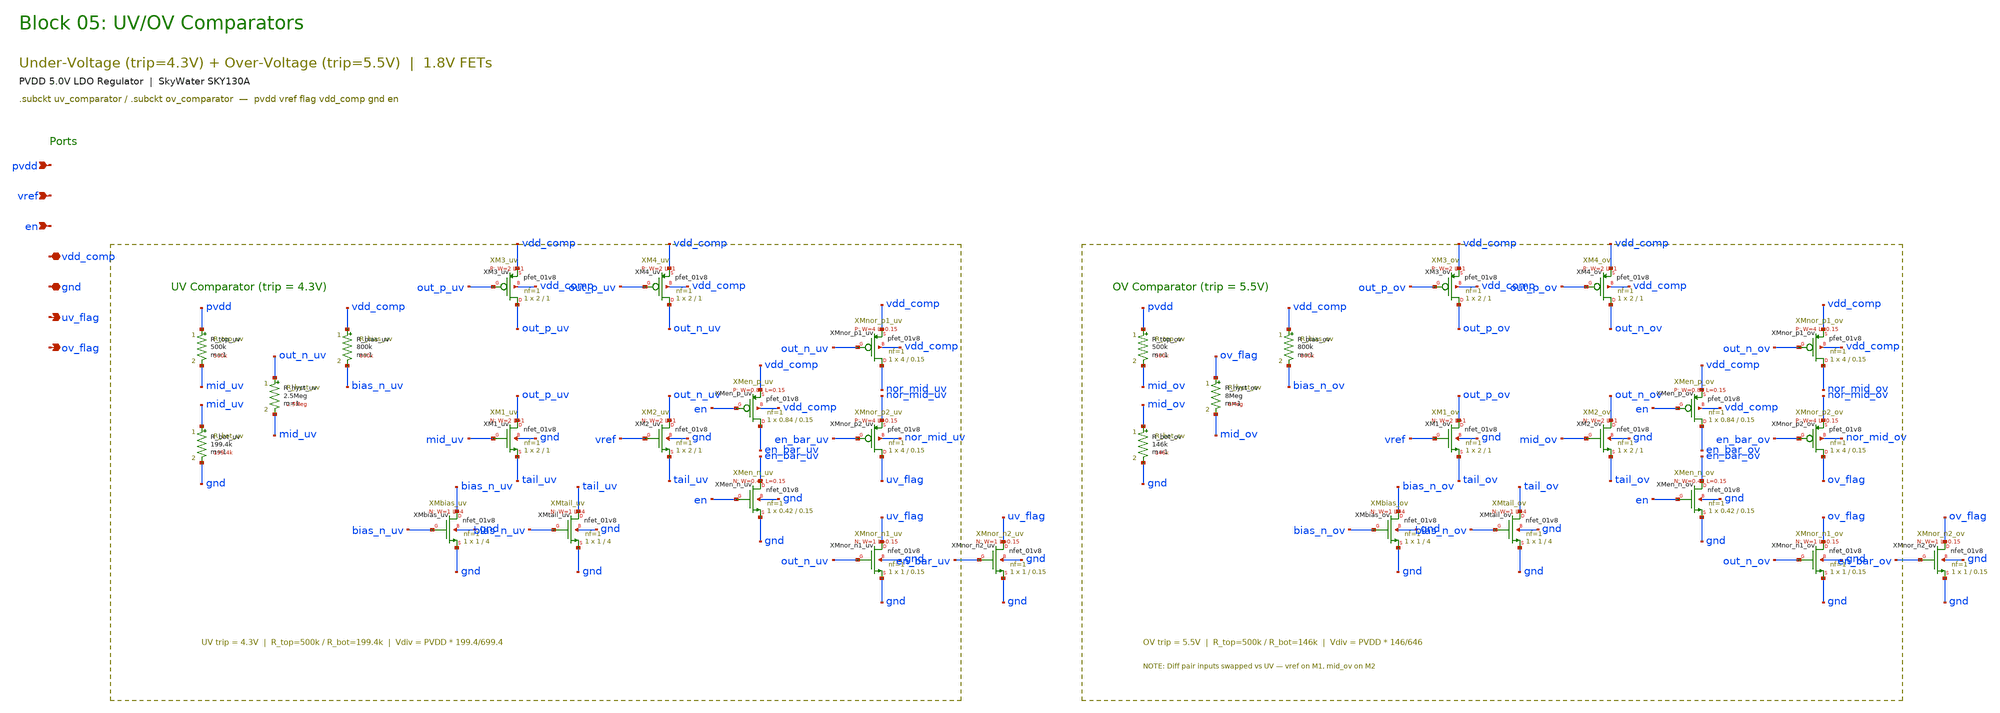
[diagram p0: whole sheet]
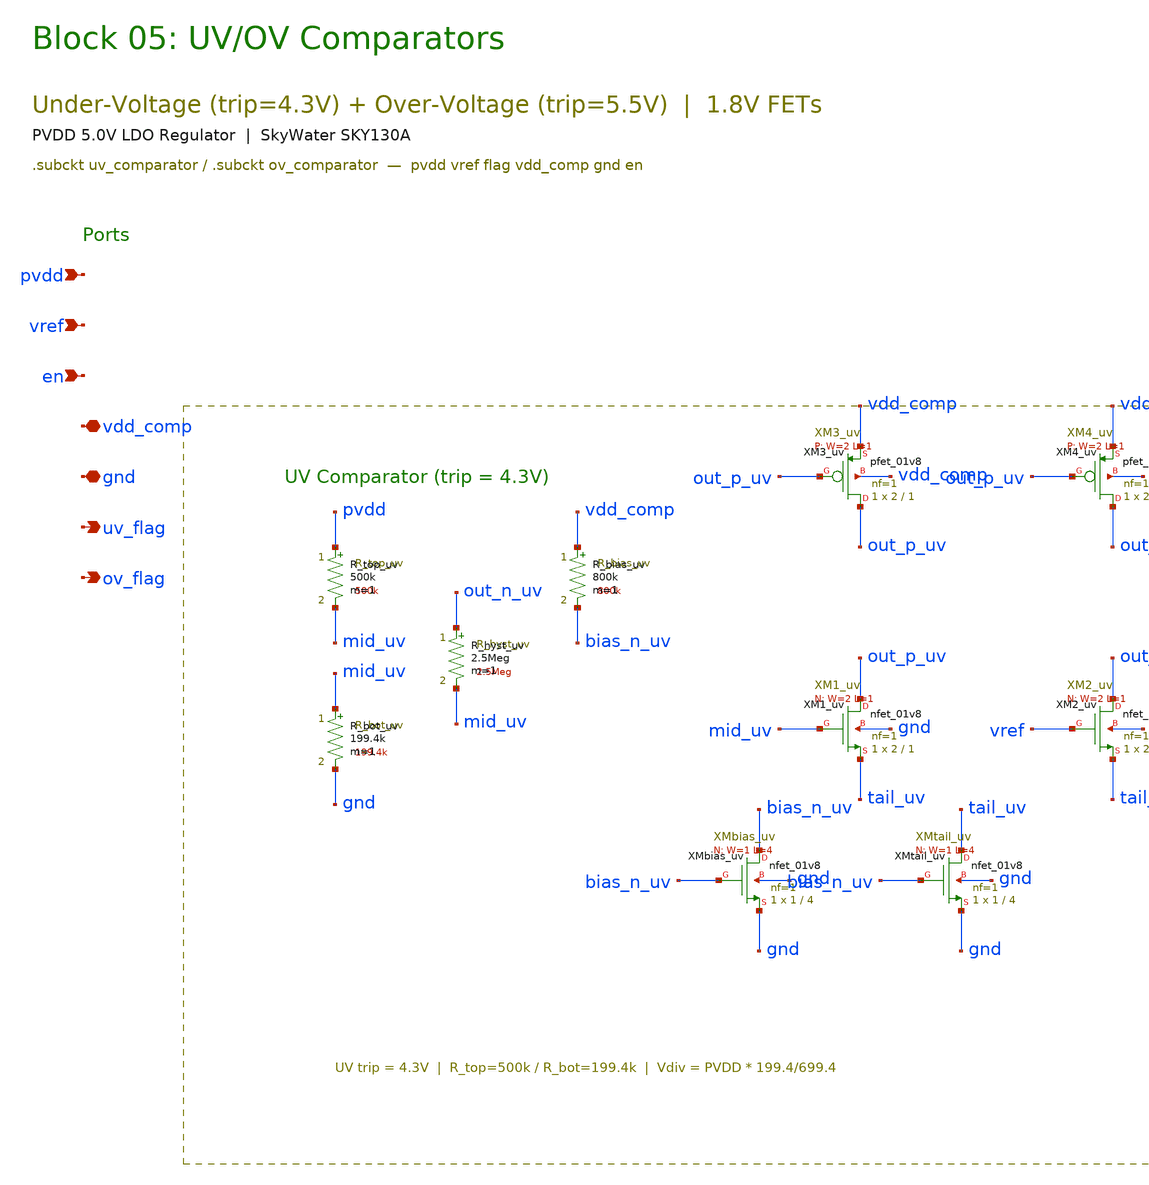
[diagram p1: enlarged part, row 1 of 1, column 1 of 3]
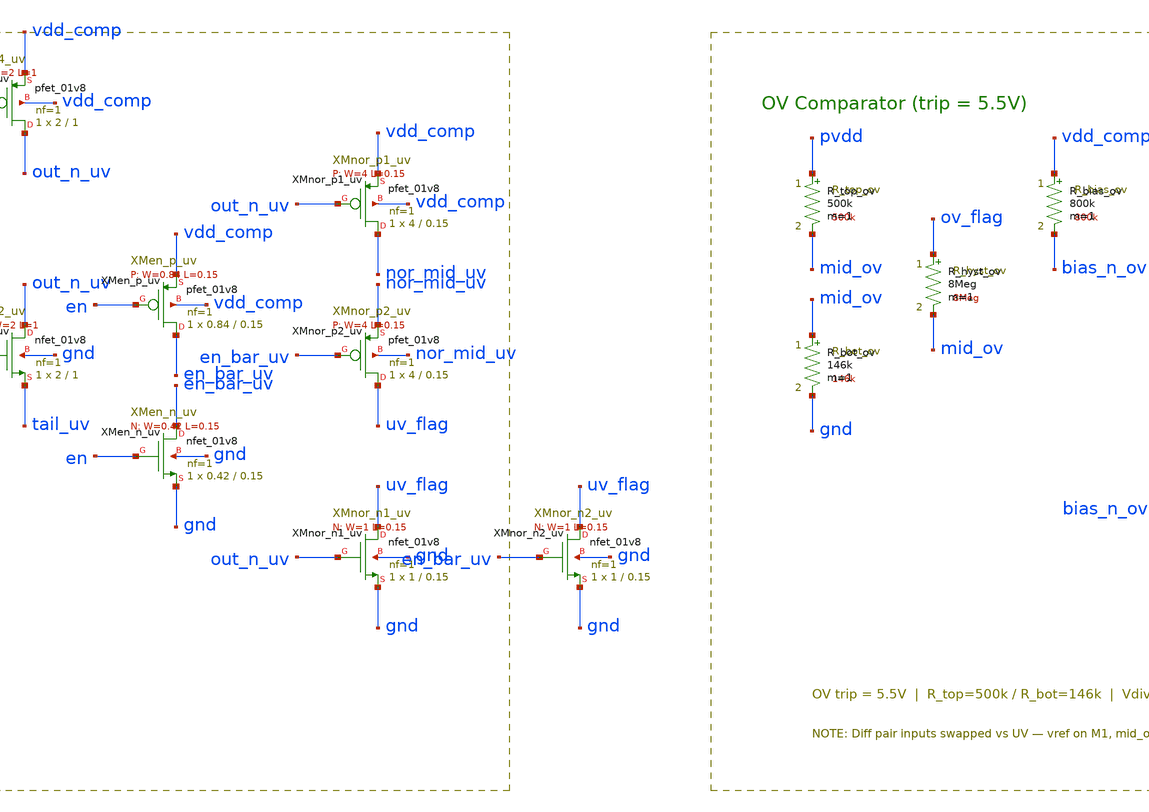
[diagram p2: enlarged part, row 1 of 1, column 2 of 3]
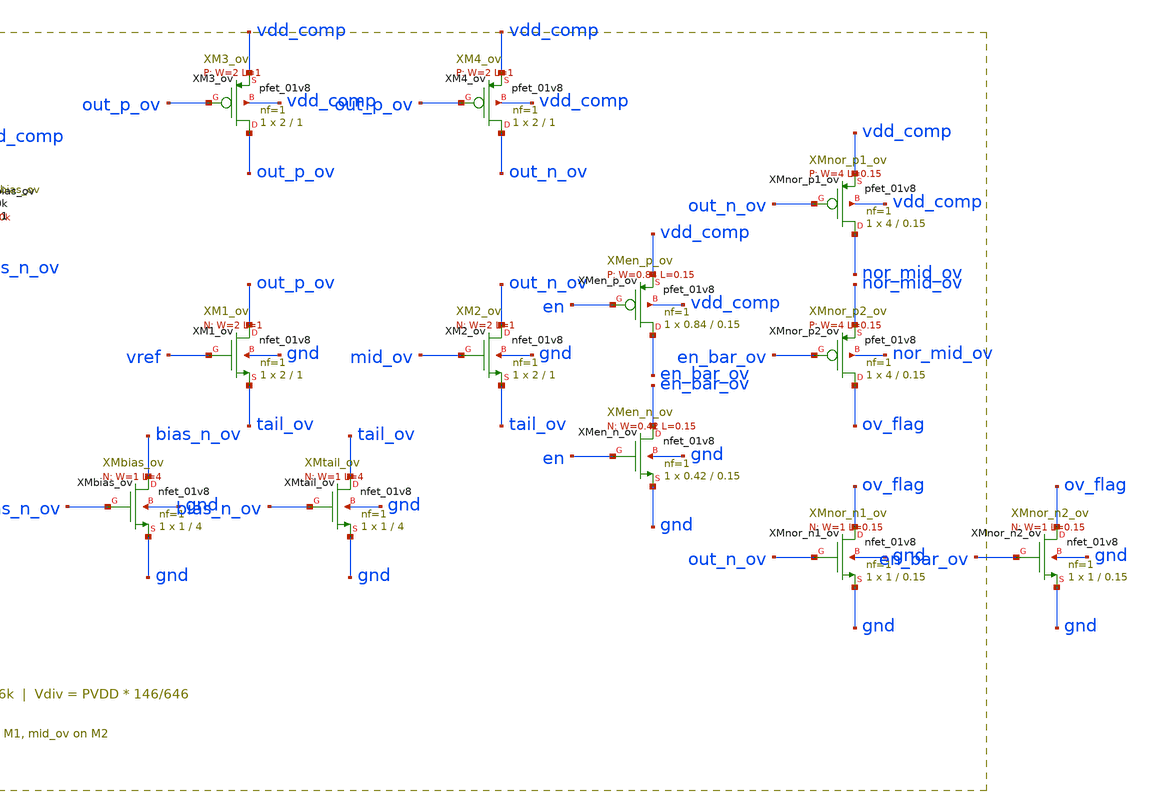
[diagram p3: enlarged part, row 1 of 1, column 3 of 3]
** sch_path: pvdd_regulator/10_top_integration/schematics/pvdd_05_uv_ov.sch
**.subckt pvdd_05_uv_ov pvdd vref en vdd_comp gnd uv_flag ov_flag
*.ipin pvdd
*.ipin vref
*.ipin en
*.iopin vdd_comp
*.iopin gnd
*.opin uv_flag
*.opin ov_flag
R_top_uv pvdd mid_uv 500k m=1
R_bot_uv mid_uv gnd 199.4k m=1
R_hyst_uv out_n_uv mid_uv 2.5Meg m=1
R_bias_uv vdd_comp bias_n_uv 800k m=1
XXMbias_uv bias_n_uv bias_n_uv gnd gnd sky130_fd_pr__nfet_01v8 L=4 W=1 nf=1 ad='int((1 + 1)/2) * 1 / 1 * 0.29'
+ as='int((1 + 2)/2) * 1 / 1 * 0.29' pd='2*int((1 + 1)/2) * (1 / 1 + 0.29)' ps='2*int((1 + 2)/2) * (1 / 1 + 0.29)'
+ nrd='0.29 / 1 ' nrs='0.29 / 1 ' sa=0 sb=0 sd=0 mult=1 m=1
XXMtail_uv tail_uv bias_n_uv gnd gnd sky130_fd_pr__nfet_01v8 L=4 W=1 nf=1 ad='int((1 + 1)/2) * 1 / 1 * 0.29'
+ as='int((1 + 2)/2) * 1 / 1 * 0.29' pd='2*int((1 + 1)/2) * (1 / 1 + 0.29)' ps='2*int((1 + 2)/2) * (1 / 1 + 0.29)'
+ nrd='0.29 / 1 ' nrs='0.29 / 1 ' sa=0 sb=0 sd=0 mult=1 m=1
XXM1_uv out_p_uv mid_uv tail_uv gnd sky130_fd_pr__nfet_01v8 L=1 W=2 nf=1 ad='int((1 + 1)/2) * 2 / 1 * 0.29'
+ as='int((1 + 2)/2) * 2 / 1 * 0.29' pd='2*int((1 + 1)/2) * (2 / 1 + 0.29)' ps='2*int((1 + 2)/2) * (2 / 1 + 0.29)'
+ nrd='0.29 / 2 ' nrs='0.29 / 2 ' sa=0 sb=0 sd=0 mult=1 m=1
XXM2_uv out_n_uv vref tail_uv gnd sky130_fd_pr__nfet_01v8 L=1 W=2 nf=1 ad='int((1 + 1)/2) * 2 / 1 * 0.29'
+ as='int((1 + 2)/2) * 2 / 1 * 0.29' pd='2*int((1 + 1)/2) * (2 / 1 + 0.29)' ps='2*int((1 + 2)/2) * (2 / 1 + 0.29)'
+ nrd='0.29 / 2 ' nrs='0.29 / 2 ' sa=0 sb=0 sd=0 mult=1 m=1
XXM3_uv out_p_uv out_p_uv vdd_comp vdd_comp sky130_fd_pr__pfet_01v8 L=1 W=2 nf=1 ad='int((nf+1)/2) * W/nf * 0.29'
+ as='int((nf+2)/2) * W/nf * 0.29' pd='2*int((nf+1)/2) * (W/nf + 0.29)' ps='2*int((nf+2)/2) * (W/nf + 0.29)'
+ nrd='0.29 / W' nrs='0.29 / W' sa=0 sb=0 sd=0 mult=1 m=1
XXM4_uv out_n_uv out_p_uv vdd_comp vdd_comp sky130_fd_pr__pfet_01v8 L=1 W=2 nf=1 ad='int((nf+1)/2) * W/nf * 0.29'
+ as='int((nf+2)/2) * W/nf * 0.29' pd='2*int((nf+1)/2) * (W/nf + 0.29)' ps='2*int((nf+2)/2) * (W/nf + 0.29)'
+ nrd='0.29 / W' nrs='0.29 / W' sa=0 sb=0 sd=0 mult=1 m=1
XXMen_n_uv en_bar_uv en gnd gnd sky130_fd_pr__nfet_01v8 L=0.15 W=0.42 nf=1 ad='int((1 + 1)/2) * 0.42 / 1 * 0.29'
+ as='int((1 + 2)/2) * 0.42 / 1 * 0.29' pd='2*int((1 + 1)/2) * (0.42 / 1 + 0.29)' ps='2*int((1 + 2)/2) * (0.42 / 1 + 0.29)'
+ nrd='0.29 / 0.42 ' nrs='0.29 / 0.42 ' sa=0 sb=0 sd=0 mult=1 m=1
XXMen_p_uv en_bar_uv en vdd_comp vdd_comp sky130_fd_pr__pfet_01v8 L=0.15 W=0.84 nf=1 ad='int((nf+1)/2) * W/nf * 0.29'
+ as='int((nf+2)/2) * W/nf * 0.29' pd='2*int((nf+1)/2) * (W/nf + 0.29)' ps='2*int((nf+2)/2) * (W/nf + 0.29)'
+ nrd='0.29 / W' nrs='0.29 / W' sa=0 sb=0 sd=0 mult=1 m=1
XXMnor_p1_uv nor_mid_uv out_n_uv vdd_comp vdd_comp sky130_fd_pr__pfet_01v8 L=0.15 W=4 nf=1 ad='int((nf+1)/2) * W/nf * 0.29'
+ as='int((nf+2)/2) * W/nf * 0.29' pd='2*int((nf+1)/2) * (W/nf + 0.29)' ps='2*int((nf+2)/2) * (W/nf + 0.29)'
+ nrd='0.29 / W' nrs='0.29 / W' sa=0 sb=0 sd=0 mult=1 m=1
XXMnor_p2_uv uv_flag en_bar_uv nor_mid_uv nor_mid_uv sky130_fd_pr__pfet_01v8 L=0.15 W=4 nf=1 ad='int((nf+1)/2) * W/nf * 0.29'
+ as='int((nf+2)/2) * W/nf * 0.29' pd='2*int((nf+1)/2) * (W/nf + 0.29)' ps='2*int((nf+2)/2) * (W/nf + 0.29)'
+ nrd='0.29 / W' nrs='0.29 / W' sa=0 sb=0 sd=0 mult=1 m=1
XXMnor_n1_uv uv_flag out_n_uv gnd gnd sky130_fd_pr__nfet_01v8 L=0.15 W=1 nf=1 ad='int((1 + 1)/2) * 1 / 1 * 0.29'
+ as='int((1 + 2)/2) * 1 / 1 * 0.29' pd='2*int((1 + 1)/2) * (1 / 1 + 0.29)' ps='2*int((1 + 2)/2) * (1 / 1 + 0.29)'
+ nrd='0.29 / 1 ' nrs='0.29 / 1 ' sa=0 sb=0 sd=0 mult=1 m=1
XXMnor_n2_uv uv_flag en_bar_uv gnd gnd sky130_fd_pr__nfet_01v8 L=0.15 W=1 nf=1 ad='int((1 + 1)/2) * 1 / 1 * 0.29'
+ as='int((1 + 2)/2) * 1 / 1 * 0.29' pd='2*int((1 + 1)/2) * (1 / 1 + 0.29)' ps='2*int((1 + 2)/2) * (1 / 1 + 0.29)'
+ nrd='0.29 / 1 ' nrs='0.29 / 1 ' sa=0 sb=0 sd=0 mult=1 m=1
R_top_ov pvdd mid_ov 500k m=1
R_bot_ov mid_ov gnd 146k m=1
R_hyst_ov ov_flag mid_ov 8Meg m=1
R_bias_ov vdd_comp bias_n_ov 800k m=1
XXMbias_ov bias_n_ov bias_n_ov gnd gnd sky130_fd_pr__nfet_01v8 L=4 W=1 nf=1 ad='int((1 + 1)/2) * 1 / 1 * 0.29'
+ as='int((1 + 2)/2) * 1 / 1 * 0.29' pd='2*int((1 + 1)/2) * (1 / 1 + 0.29)' ps='2*int((1 + 2)/2) * (1 / 1 + 0.29)'
+ nrd='0.29 / 1 ' nrs='0.29 / 1 ' sa=0 sb=0 sd=0 mult=1 m=1
XXMtail_ov tail_ov bias_n_ov gnd gnd sky130_fd_pr__nfet_01v8 L=4 W=1 nf=1 ad='int((1 + 1)/2) * 1 / 1 * 0.29'
+ as='int((1 + 2)/2) * 1 / 1 * 0.29' pd='2*int((1 + 1)/2) * (1 / 1 + 0.29)' ps='2*int((1 + 2)/2) * (1 / 1 + 0.29)'
+ nrd='0.29 / 1 ' nrs='0.29 / 1 ' sa=0 sb=0 sd=0 mult=1 m=1
XXM1_ov out_p_ov vref tail_ov gnd sky130_fd_pr__nfet_01v8 L=1 W=2 nf=1 ad='int((1 + 1)/2) * 2 / 1 * 0.29'
+ as='int((1 + 2)/2) * 2 / 1 * 0.29' pd='2*int((1 + 1)/2) * (2 / 1 + 0.29)' ps='2*int((1 + 2)/2) * (2 / 1 + 0.29)'
+ nrd='0.29 / 2 ' nrs='0.29 / 2 ' sa=0 sb=0 sd=0 mult=1 m=1
XXM2_ov out_n_ov mid_ov tail_ov gnd sky130_fd_pr__nfet_01v8 L=1 W=2 nf=1 ad='int((1 + 1)/2) * 2 / 1 * 0.29'
+ as='int((1 + 2)/2) * 2 / 1 * 0.29' pd='2*int((1 + 1)/2) * (2 / 1 + 0.29)' ps='2*int((1 + 2)/2) * (2 / 1 + 0.29)'
+ nrd='0.29 / 2 ' nrs='0.29 / 2 ' sa=0 sb=0 sd=0 mult=1 m=1
XXM3_ov out_p_ov out_p_ov vdd_comp vdd_comp sky130_fd_pr__pfet_01v8 L=1 W=2 nf=1 ad='int((nf+1)/2) * W/nf * 0.29'
+ as='int((nf+2)/2) * W/nf * 0.29' pd='2*int((nf+1)/2) * (W/nf + 0.29)' ps='2*int((nf+2)/2) * (W/nf + 0.29)'
+ nrd='0.29 / W' nrs='0.29 / W' sa=0 sb=0 sd=0 mult=1 m=1
XXM4_ov out_n_ov out_p_ov vdd_comp vdd_comp sky130_fd_pr__pfet_01v8 L=1 W=2 nf=1 ad='int((nf+1)/2) * W/nf * 0.29'
+ as='int((nf+2)/2) * W/nf * 0.29' pd='2*int((nf+1)/2) * (W/nf + 0.29)' ps='2*int((nf+2)/2) * (W/nf + 0.29)'
+ nrd='0.29 / W' nrs='0.29 / W' sa=0 sb=0 sd=0 mult=1 m=1
XXMen_n_ov en_bar_ov en gnd gnd sky130_fd_pr__nfet_01v8 L=0.15 W=0.42 nf=1 ad='int((1 + 1)/2) * 0.42 / 1 * 0.29'
+ as='int((1 + 2)/2) * 0.42 / 1 * 0.29' pd='2*int((1 + 1)/2) * (0.42 / 1 + 0.29)' ps='2*int((1 + 2)/2) * (0.42 / 1 + 0.29)'
+ nrd='0.29 / 0.42 ' nrs='0.29 / 0.42 ' sa=0 sb=0 sd=0 mult=1 m=1
XXMen_p_ov en_bar_ov en vdd_comp vdd_comp sky130_fd_pr__pfet_01v8 L=0.15 W=0.84 nf=1 ad='int((nf+1)/2) * W/nf * 0.29'
+ as='int((nf+2)/2) * W/nf * 0.29' pd='2*int((nf+1)/2) * (W/nf + 0.29)' ps='2*int((nf+2)/2) * (W/nf + 0.29)'
+ nrd='0.29 / W' nrs='0.29 / W' sa=0 sb=0 sd=0 mult=1 m=1
XXMnor_p1_ov nor_mid_ov out_n_ov vdd_comp vdd_comp sky130_fd_pr__pfet_01v8 L=0.15 W=4 nf=1 ad='int((nf+1)/2) * W/nf * 0.29'
+ as='int((nf+2)/2) * W/nf * 0.29' pd='2*int((nf+1)/2) * (W/nf + 0.29)' ps='2*int((nf+2)/2) * (W/nf + 0.29)'
+ nrd='0.29 / W' nrs='0.29 / W' sa=0 sb=0 sd=0 mult=1 m=1
XXMnor_p2_ov ov_flag en_bar_ov nor_mid_ov nor_mid_ov sky130_fd_pr__pfet_01v8 L=0.15 W=4 nf=1 ad='int((nf+1)/2) * W/nf * 0.29'
+ as='int((nf+2)/2) * W/nf * 0.29' pd='2*int((nf+1)/2) * (W/nf + 0.29)' ps='2*int((nf+2)/2) * (W/nf + 0.29)'
+ nrd='0.29 / W' nrs='0.29 / W' sa=0 sb=0 sd=0 mult=1 m=1
XXMnor_n1_ov ov_flag out_n_ov gnd gnd sky130_fd_pr__nfet_01v8 L=0.15 W=1 nf=1 ad='int((1 + 1)/2) * 1 / 1 * 0.29'
+ as='int((1 + 2)/2) * 1 / 1 * 0.29' pd='2*int((1 + 1)/2) * (1 / 1 + 0.29)' ps='2*int((1 + 2)/2) * (1 / 1 + 0.29)'
+ nrd='0.29 / 1 ' nrs='0.29 / 1 ' sa=0 sb=0 sd=0 mult=1 m=1
XXMnor_n2_ov ov_flag en_bar_ov gnd gnd sky130_fd_pr__nfet_01v8 L=0.15 W=1 nf=1 ad='int((1 + 1)/2) * 1 / 1 * 0.29'
+ as='int((1 + 2)/2) * 1 / 1 * 0.29' pd='2*int((1 + 1)/2) * (1 / 1 + 0.29)' ps='2*int((1 + 2)/2) * (1 / 1 + 0.29)'
+ nrd='0.29 / 1 ' nrs='0.29 / 1 ' sa=0 sb=0 sd=0 mult=1 m=1
**.ends
.end
